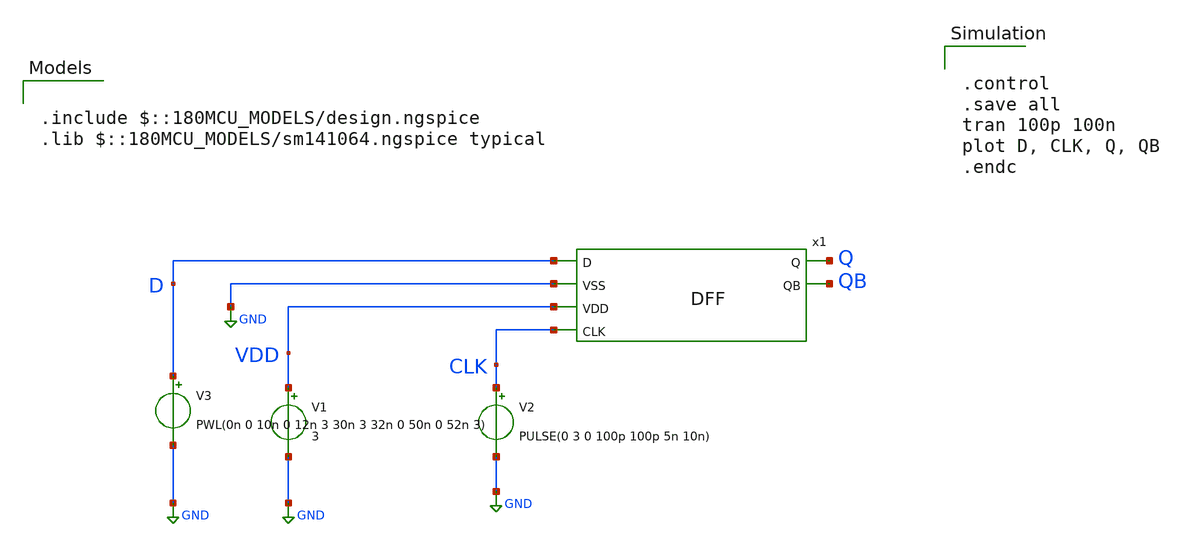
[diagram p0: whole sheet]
** sch_path: designs/libs/core_analog/DFF/dff_tb.sch
**.subckt dff_tb
V1 VDD GND 3
V2 CLK GND PULSE(0 3 0 100p 100p 5n 10n)
V3 D GND PWL(0n 0 10n 0 12n 3 30n 3 32n 0 50n 0 52n 3)
x1 D GND VDD Q CLK QB DFF
**** begin user architecture code

.include $::180MCU_MODELS/design.ngspice
.lib $::180MCU_MODELS/sm141064.ngspice typical



.control
.save all
tran 100p 100n
plot D, CLK, Q, QB
.endc


**** end user architecture code
**.ends
.GLOBAL GND
.end
